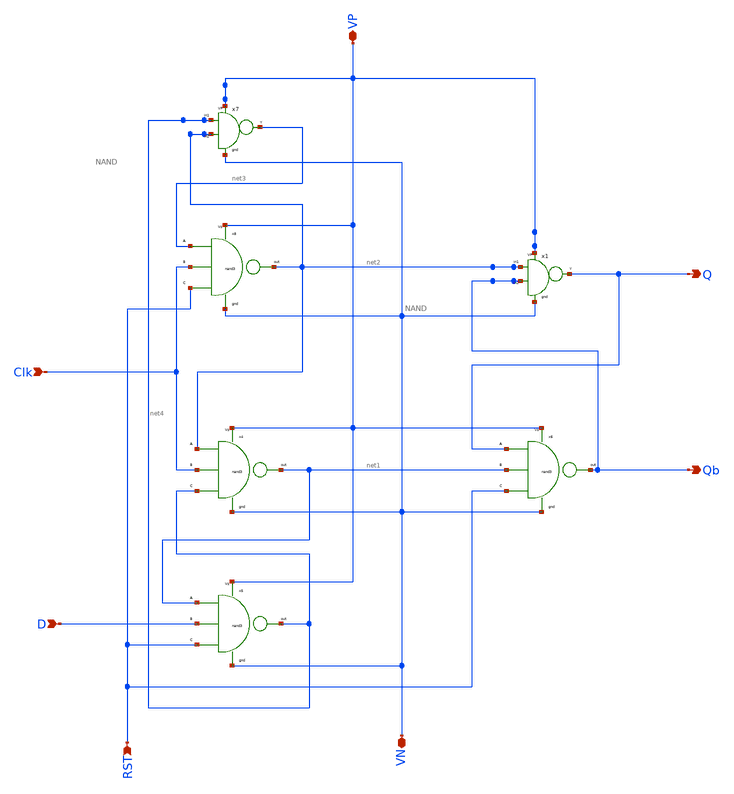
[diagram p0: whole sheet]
** sch_path: component/FlipFlops/DFF1.sch
**.subckt DFF1 Q VN VP Clk D RST Qb
*.opin Q
*.iopin VN
*.iopin VP
*.ipin Clk
*.ipin D
*.ipin RST
*.opin Qb
x7 net2 net4 net3 VP VN NAND
x8 net3 Clk RST VP VN net2 NAND3
x6 Q net1 RST VP VN Qb NAND3
x4 net2 Clk net4 VP VN net1 NAND3
x5 net1 D RST VP VN net4 NAND3
x1 Qb net2 Q VP VN NAND
**.ends

* expanding   symbol:  component/NAND2/NAND.sym # of pins=5
** sym_path: component/NAND2/NAND.sym
** sch_path: component/NAND2/NAND.sch
.subckt NAND B A Y VP VN
*.iopin VP
*.ipin A
*.ipin B
*.opin Y
*.iopin VN
XM1 Y A VP VP sky130_fd_pr__pfet_01v8 L=0.15 W=1.26 nf=1 ad='int((nf+1)/2) * W/nf * 0.29' as='int((nf+2)/2) * W/nf * 0.29'
+ pd='2*int((nf+1)/2) * (W/nf + 0.29)' ps='2*int((nf+2)/2) * (W/nf + 0.29)' nrd='0.29 / W' nrs='0.29 / W'
+ sa=0 sb=0 sd=0 mult=1 m=1
XM2 Y B VP VP sky130_fd_pr__pfet_01v8 L=0.15 W=1.26 nf=1 ad='int((nf+1)/2) * W/nf * 0.29' as='int((nf+2)/2) * W/nf * 0.29'
+ pd='2*int((nf+1)/2) * (W/nf + 0.29)' ps='2*int((nf+2)/2) * (W/nf + 0.29)' nrd='0.29 / W' nrs='0.29 / W'
+ sa=0 sb=0 sd=0 mult=1 m=1
XM3 Y A net1 net1 sky130_fd_pr__nfet_01v8 L=0.15 W=0.84 nf=1 ad='int((nf+1)/2) * W/nf * 0.29' as='int((nf+2)/2) * W/nf * 0.29'
+ pd='2*int((nf+1)/2) * (W/nf + 0.29)' ps='2*int((nf+2)/2) * (W/nf + 0.29)' nrd='0.29 / W' nrs='0.29 / W'
+ sa=0 sb=0 sd=0 mult=1 m=1
XM4 net1 B VN VN sky130_fd_pr__nfet_01v8 L=0.15 W=0.84 nf=1 ad='int((nf+1)/2) * W/nf * 0.29' as='int((nf+2)/2) * W/nf * 0.29'
+ pd='2*int((nf+1)/2) * (W/nf + 0.29)' ps='2*int((nf+2)/2) * (W/nf + 0.29)' nrd='0.29 / W' nrs='0.29 / W'
+ sa=0 sb=0 sd=0 mult=1 m=1
.ends


* expanding   symbol:  component/NAND3/NAND3.sym # of pins=6
** sym_path: component/NAND3/NAND3.sym
** sch_path: component/NAND3/NAND3.sch
.subckt NAND3 A B C VP VN Y
*.iopin VP
*.iopin VN
*.ipin A
*.ipin B
*.ipin C
*.opin Y
XM1 Y A net1 VN sky130_fd_pr__nfet_01v8 L=0.15 W=1.26 nf=1 ad='int((nf+1)/2) * W/nf * 0.29' as='int((nf+2)/2) * W/nf * 0.29'
+ pd='2*int((nf+1)/2) * (W/nf + 0.29)' ps='2*int((nf+2)/2) * (W/nf + 0.29)' nrd='0.29 / W' nrs='0.29 / W'
+ sa=0 sb=0 sd=0 mult=1 m=1
XM2 net1 B net2 VN sky130_fd_pr__nfet_01v8 L=0.15 W=1.26 nf=1 ad='int((nf+1)/2) * W/nf * 0.29' as='int((nf+2)/2) * W/nf * 0.29'
+ pd='2*int((nf+1)/2) * (W/nf + 0.29)' ps='2*int((nf+2)/2) * (W/nf + 0.29)' nrd='0.29 / W' nrs='0.29 / W'
+ sa=0 sb=0 sd=0 mult=1 m=1
XM3 net2 C VN VN sky130_fd_pr__nfet_01v8 L=0.15 W=1.26 nf=1 ad='int((nf+1)/2) * W/nf * 0.29' as='int((nf+2)/2) * W/nf * 0.29'
+ pd='2*int((nf+1)/2) * (W/nf + 0.29)' ps='2*int((nf+2)/2) * (W/nf + 0.29)' nrd='0.29 / W' nrs='0.29 / W'
+ sa=0 sb=0 sd=0 mult=1 m=1
XM4 Y A VP VP sky130_fd_pr__pfet_01v8 L=0.15 W=1.26 nf=1 ad='int((nf+1)/2) * W/nf * 0.29' as='int((nf+2)/2) * W/nf * 0.29'
+ pd='2*int((nf+1)/2) * (W/nf + 0.29)' ps='2*int((nf+2)/2) * (W/nf + 0.29)' nrd='0.29 / W' nrs='0.29 / W'
+ sa=0 sb=0 sd=0 mult=1 m=1
XM5 Y B VP VP sky130_fd_pr__pfet_01v8 L=0.15 W=1.26 nf=1 ad='int((nf+1)/2) * W/nf * 0.29' as='int((nf+2)/2) * W/nf * 0.29'
+ pd='2*int((nf+1)/2) * (W/nf + 0.29)' ps='2*int((nf+2)/2) * (W/nf + 0.29)' nrd='0.29 / W' nrs='0.29 / W'
+ sa=0 sb=0 sd=0 mult=1 m=1
XM6 Y C VP VP sky130_fd_pr__pfet_01v8 L=0.15 W=1.26 nf=1 ad='int((nf+1)/2) * W/nf * 0.29' as='int((nf+2)/2) * W/nf * 0.29'
+ pd='2*int((nf+1)/2) * (W/nf + 0.29)' ps='2*int((nf+2)/2) * (W/nf + 0.29)' nrd='0.29 / W' nrs='0.29 / W'
+ sa=0 sb=0 sd=0 mult=1 m=1
.ends

.end
